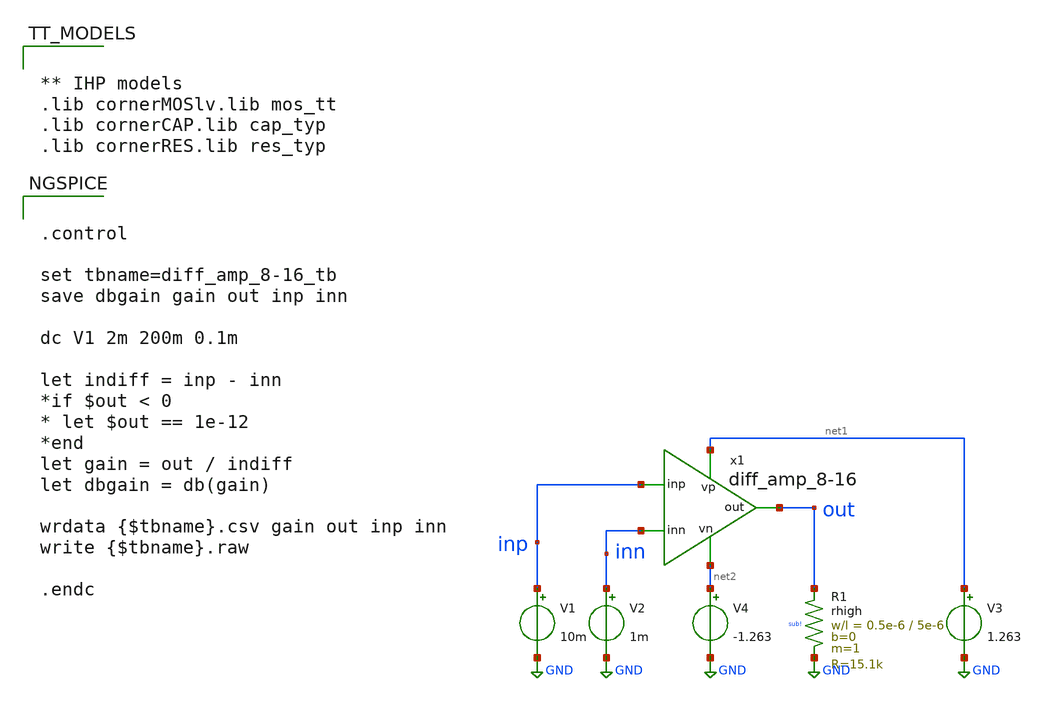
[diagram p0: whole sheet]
** sch_path: TempSensor/design_data/xschem/diff_amp_8-16_tb.sch
**.subckt diff_amp_8-16_tb
V2 inn GND 1m
V1 inp GND 10m
V3 net1 GND 1.263
x1 net1 inn inp out net2 diff_amp_8-16
XR1 out GND sub! rhigh w=0.5e-6 l=5e-6 m=1 b=0 mm_ok=1
V4 net2 GND -1.263
**** begin user architecture code


** IHP models
.lib cornerMOSlv.lib mos_tt
.lib cornerCAP.lib cap_typ
.lib cornerRES.lib res_typ




.control

set tbname=diff_amp_8-16_tb
save dbgain gain out inp inn

dc V1 2m 200m 0.1m

let indiff = inp - inn
*if $out < 0
* let $out == 1e-12
*end
let gain = out / indiff
let dbgain = db(gain)

wrdata {$tbname}.csv gain out inp inn
write {$tbname}.raw

.endc


**** end user architecture code
**.ends

* expanding   symbol:  practicing/TempSensor/design_data/xschem/diff_amp_8-16.sym # of pins=5
** sym_path: TempSensor/design_data/xschem/diff_amp_8-16.sym
** sch_path: TempSensor/design_data/xschem/diff_amp_8-16.sch
.subckt diff_amp_8-16 vp inn inp out vn
*.ipin inp
*.opin out
*.ipin inn
*.iopin vn
*.iopin vp
XM6 net10 inn net2 vn sg13_lv_nmos w=10u l=0.5u ng=1 m=1 mm_ok=1
XM5 net11 inp net2 vn sg13_lv_nmos w=10u l=0.5u ng=1 m=1 mm_ok=1
XM2 net1 net1 net4 vp sg13_lv_pmos w=10u l=2u ng=1 m=10 mm_ok=1
XM1 net4 net1 vp vp sg13_lv_pmos w=6u l=1u ng=1 m=1 mm_ok=1
XM3 net3 net1 vp vp sg13_lv_pmos w=6u l=1u ng=1 m=1 mm_ok=1
XM4 net5 net1 net3 vp sg13_lv_pmos w=10u l=2u ng=1 m=10 mm_ok=1
XM7 net5 net5 net6 vn sg13_lv_nmos w=10u l=2u ng=1 m=10 mm_ok=1
XM8 net6 net5 vn vn sg13_lv_nmos w=10u l=5u ng=1 m=1 mm_ok=1
XM9 net2 net5 net7 vn sg13_lv_nmos w=10u l=2u ng=1 m=10 mm_ok=1
XM10 net7 net5 vn vn sg13_lv_nmos w=10u l=5u ng=1 m=1 mm_ok=1
XM15 net8 net8 vn vn sg13_lv_nmos w=10u l=1.5u ng=1 m=1 mm_ok=1
XM16 net9 net8 vn vn sg13_lv_nmos w=10u l=1.5u ng=1 m=1 mm_ok=1
XM11 net10 net1 vp vp sg13_lv_pmos w=10u l=1.67u ng=1 m=1 mm_ok=1
XM12 net8 net1 net10 vp sg13_lv_pmos w=10u l=2u ng=1 m=10 mm_ok=1
XM13 net11 net1 vp vp sg13_lv_pmos w=10u l=1.67u ng=1 m=1 mm_ok=1
XM14 net9 net1 net11 vp sg13_lv_pmos w=10u l=2u ng=1 m=10 mm_ok=1
XM17 out net1 vp vp sg13_lv_pmos w=9u l=5u ng=1 m=10 mm_ok=1
XM18 out net9 vn vn sg13_lv_nmos w=10u l=0.5u ng=1 m=5 mm_ok=1
I0 net1 vn 20u
XC2 out net9 cap_cmim w=35e-6 l=35e-6 m=1 mm_ok=1
.ends

.GLOBAL GND
.end
